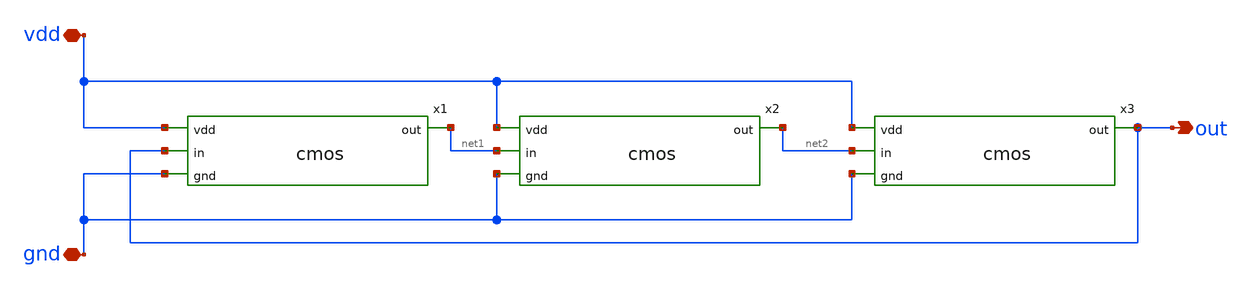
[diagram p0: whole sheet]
** sch_path: Ring Oscillator/ring-oscillator3.sch
**.subckt ring-oscillator3 vdd gnd out
*.iopin vdd
*.iopin gnd
*.opin out
x1 vdd out net1 gnd cmos
x2 vdd net1 net2 gnd cmos
x3 vdd net2 out gnd cmos
**.ends

* expanding   symbol:  /home/delviery/test-xschem/cmos.sym # of pins=4
** sym_path: CMOS inverter/cmos.sym
** sch_path: CMOS inverter/cmos.sch
.subckt cmos vdd in out gnd
*.ipin vdd
*.ipin in
*.ipin gnd
*.opin out
XM1 out in gnd gnd sky130_fd_pr__nfet_01v8 L=0.15 W=1 nf=1 ad='int((nf+1)/2) * W/nf * 0.29' as='int((nf+2)/2) * W/nf * 0.29'
+ pd='2*int((nf+1)/2) * (W/nf + 0.29)' ps='2*int((nf+2)/2) * (W/nf + 0.29)' nrd='0.29 / W' nrs='0.29 / W'
+ sa=0 sb=0 sd=0 mult=1 m=1
XM2 out in vdd vdd sky130_fd_pr__pfet_01v8 L=0.15 W=1 nf=1 ad='int((nf+1)/2) * W/nf * 0.29' as='int((nf+2)/2) * W/nf * 0.29'
+ pd='2*int((nf+1)/2) * (W/nf + 0.29)' ps='2*int((nf+2)/2) * (W/nf + 0.29)' nrd='0.29 / W' nrs='0.29 / W'
+ sa=0 sb=0 sd=0 mult=1 m=1
.ends

.end
